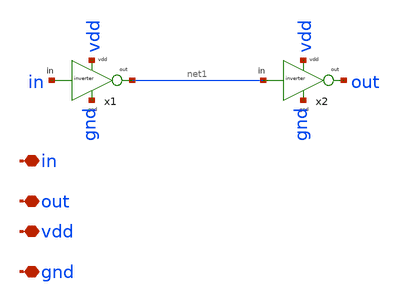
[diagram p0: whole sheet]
** sch_path: Clock_gen_using_transistor_hv/buffer.sch
**.subckt buffer in out vdd gnd
*.iopin in
*.iopin out
*.iopin vdd
*.iopin gnd
x1 in net1 vdd gnd inverter
x2 net1 out vdd gnd inverter
**.ends

* expanding   symbol:
*+  /home/designer/shared/uni_cass/final_Design_file/Clock_gen_using_transistor_hv/inverter.sym # of pins=4
** sym_path: /home/designer/shared/uni_cass/final_Design_file/Clock_gen_using_transistor_hv/inverter.sym
** sch_path: /home/designer/shared/uni_cass/final_Design_file/Clock_gen_using_transistor_hv/inverter.sch
.subckt inverter in out vdd gnd
*.iopin in
*.iopin vdd
*.iopin out
*.iopin gnd
XM3 out in vdd vdd sg13_hv_pmos w=2u l=2u ng=1 m=1 mm_ok=1
XM1 out in gnd gnd sg13_hv_nmos w=1u l=1u ng=1 m=1 mm_ok=1
.ends

.end
